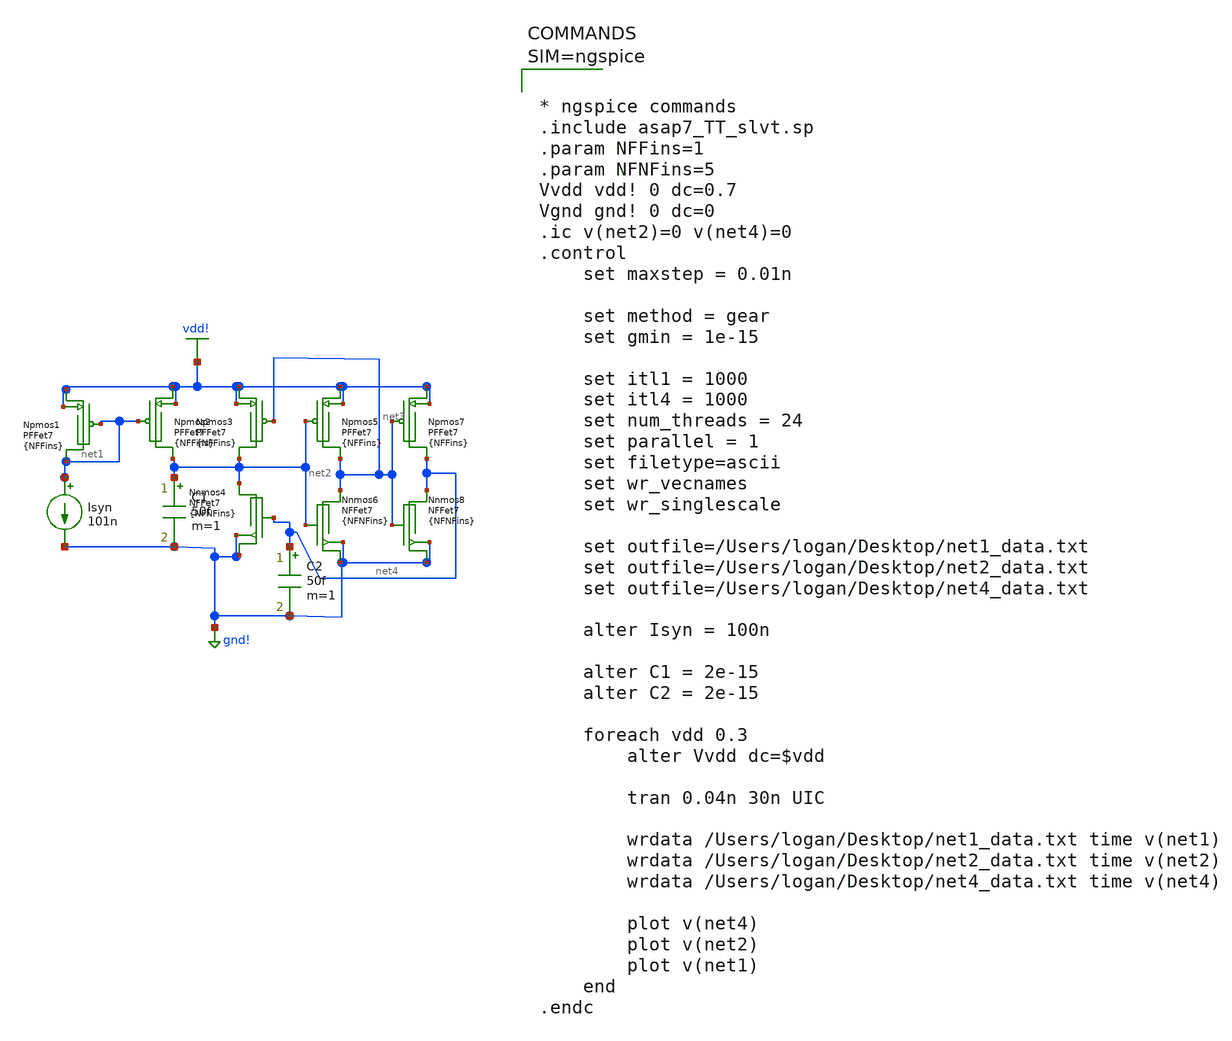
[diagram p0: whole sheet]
** sch_path: SimulationModeling/BesrourPlotting.sch
**.subckt BesrourPlotting
Npmos2 vdd! net1 net2 vdd! BSIMCMG_osdi_P nfin={NFFins}
Npmos5 vdd! net2 net3 vdd! BSIMCMG_osdi_P nfin={NFFins}
Npmos7 vdd! net3 net4 vdd! BSIMCMG_osdi_P nfin={NFFins}
Nnmos6 gnd! net2 net3 gnd! BSIMCMG_osdi_N nfin={NFNFins}
Nnmos8 gnd! net3 net4 gnd! BSIMCMG_osdi_N nfin={NFNFins}
C2 net4 gnd! 50f m=1
C1 net2 gnd! 50f m=1
Npmos1 vdd! net1 net1 vdd! BSIMCMG_osdi_P nfin={NFFins}
Npmos3 vdd! net3 net2 vdd! BSIMCMG_osdi_P nfin={NFFins}
Nnmos4 gnd! net4 net2 gnd! BSIMCMG_osdi_N nfin={NFNFins}
Isyn net1 gnd! 101n
**** begin user architecture code



* ngspice commands
.include asap7_TT_slvt.sp
.param NFFins=1
.param NFNFins=5
Vvdd vdd! 0 dc=0.7
Vgnd gnd! 0 dc=0
.ic v(net2)=0 v(net4)=0
.control
    set maxstep = 0.01n

    set method = gear
    set gmin = 1e-15

    set itl1 = 1000
    set itl4 = 1000
    set num_threads = 24
    set parallel = 1
    set filetype=ascii
    set wr_vecnames
    set wr_singlescale

    set outfile=/Users/logan/Desktop/net1_data.txt
    set outfile=/Users/logan/Desktop/net2_data.txt
    set outfile=/Users/logan/Desktop/net4_data.txt

    alter Isyn = 100n

    alter C1 = 2e-15
    alter C2 = 2e-15

    foreach vdd 0.3
        alter Vvdd dc=$vdd

        tran 0.04n 30n UIC

        wrdata /Users/logan/Desktop/net1_data.txt time v(net1)
        wrdata /Users/logan/Desktop/net2_data.txt time v(net2)
        wrdata /Users/logan/Desktop/net4_data.txt time v(net4)

        plot v(net4)
        plot v(net2)
        plot v(net1)
    end
.endc



**** end user architecture code
**.ends
.GLOBAL vdd!
.GLOBAL gnd!
.end
